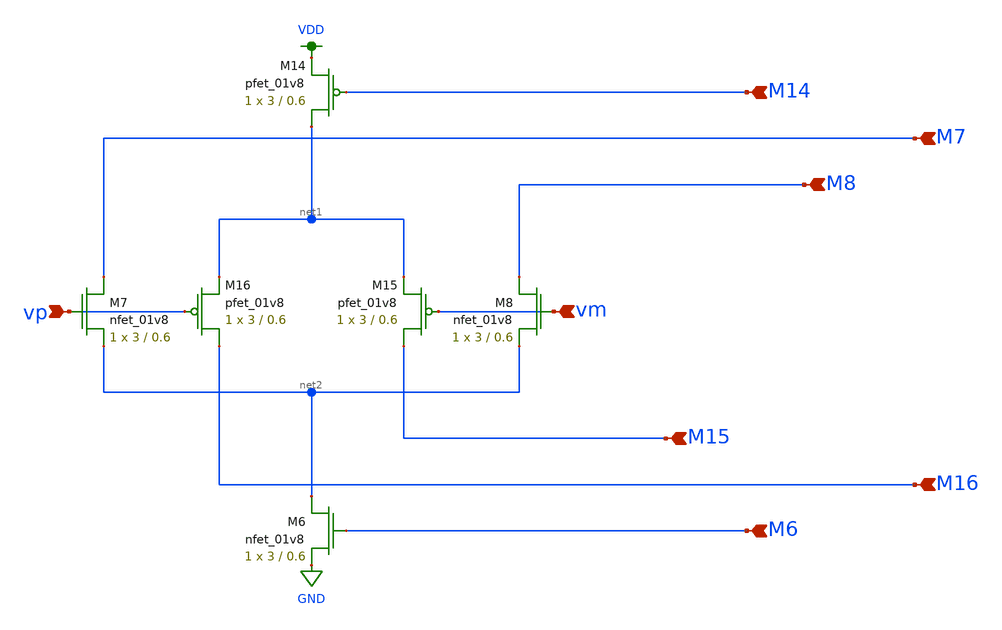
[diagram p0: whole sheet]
** sch_path: schematic/selfbiasedcascode2stage_diff_pair.sch
**.subckt selfbiasedcascode2stage_diff_pair vp vm M15 M16 M14 M7 M8 M6
*.ipin vp
*.ipin vm
*.ipin M15
*.ipin M16
*.ipin M14
*.ipin M7
*.ipin M8
*.ipin M6
XM6 net2 M6 GND GND sky130_fd_pr__nfet_01v8 L=0.6 W=3 nf=1 ad='int((nf+1)/2) * W/nf * 0.29' as='int((nf+2)/2) * W/nf * 0.29'
+ pd='2*int((nf+1)/2) * (W/nf + 0.29)' ps='2*int((nf+2)/2) * (W/nf + 0.29)' nrd='0.29 / W' nrs='0.29 / W'
+ sa=0 sb=0 sd=0 mult=1 m=1
XM7 M7 vp net2 GND sky130_fd_pr__nfet_01v8 L=0.6 W=3 nf=1 ad='int((nf+1)/2) * W/nf * 0.29' as='int((nf+2)/2) * W/nf * 0.29'
+ pd='2*int((nf+1)/2) * (W/nf + 0.29)' ps='2*int((nf+2)/2) * (W/nf + 0.29)' nrd='0.29 / W' nrs='0.29 / W'
+ sa=0 sb=0 sd=0 mult=1 m=1
XM8 M8 vm net2 GND sky130_fd_pr__nfet_01v8 L=0.6 W=3 nf=1 ad='int((nf+1)/2) * W/nf * 0.29' as='int((nf+2)/2) * W/nf * 0.29'
+ pd='2*int((nf+1)/2) * (W/nf + 0.29)' ps='2*int((nf+2)/2) * (W/nf + 0.29)' nrd='0.29 / W' nrs='0.29 / W'
+ sa=0 sb=0 sd=0 mult=1 m=1
XM14 net1 M14 VDD VDD sky130_fd_pr__pfet_01v8 L=0.6 W=3 nf=1 ad='int((nf+1)/2) * W/nf * 0.29' as='int((nf+2)/2) * W/nf * 0.29'
+ pd='2*int((nf+1)/2) * (W/nf + 0.29)' ps='2*int((nf+2)/2) * (W/nf + 0.29)' nrd='0.29 / W' nrs='0.29 / W'
+ sa=0 sb=0 sd=0 mult=1 m=1
XM15 M15 vm net1 VDD sky130_fd_pr__pfet_01v8 L=0.6 W=3 nf=1 ad='int((nf+1)/2) * W/nf * 0.29' as='int((nf+2)/2) * W/nf * 0.29'
+ pd='2*int((nf+1)/2) * (W/nf + 0.29)' ps='2*int((nf+2)/2) * (W/nf + 0.29)' nrd='0.29 / W' nrs='0.29 / W'
+ sa=0 sb=0 sd=0 mult=1 m=1
XM16 M16 vp net1 VDD sky130_fd_pr__pfet_01v8 L=0.6 W=3 nf=1 ad='int((nf+1)/2) * W/nf * 0.29' as='int((nf+2)/2) * W/nf * 0.29'
+ pd='2*int((nf+1)/2) * (W/nf + 0.29)' ps='2*int((nf+2)/2) * (W/nf + 0.29)' nrd='0.29 / W' nrs='0.29 / W'
+ sa=0 sb=0 sd=0 mult=1 m=1
**.ends
.GLOBAL GND
.GLOBAL VDD
.end
